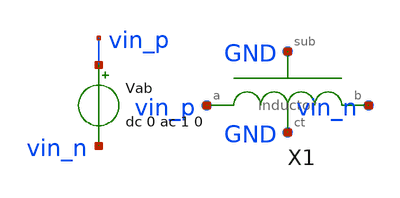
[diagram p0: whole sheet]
** sch_path: tb/inductor/tb_yparam_diff.sch
**.subckt tb_yparam_diff
X1 GND vin_p GND vin_n inductor
Vab vin_p vin_n dc 0 ac 1 0
**** begin user architecture code


.include 'models_dir'/design.spice
.option TEMP='temperature'
.option warn=1
.control
save all
ac dec 100 1meg 20g
let ydiff = i(vab)/(v(vin_p)-v(vin_n))
let ydiff_re = real(ydiff)
let ydiff_im = imag(ydiff)
set wr_singlescale
wrdata 'simpath'/'filename'_'N'.data frequency ydiff_re ydiff_im
quit
.endc


**** end user architecture code
**.ends
.end
